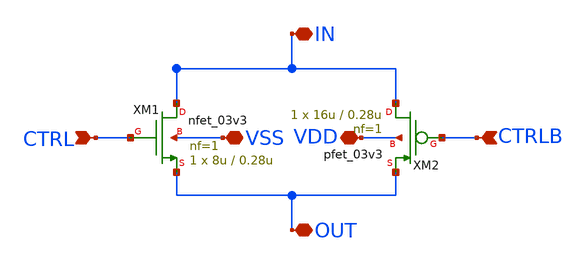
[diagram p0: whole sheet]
** sch_path: designs/libs/core_matchmaker/tg_switch/tg_switch_nmos8u_pmos16u.sch
**.subckt tg_switch_nmos8u_pmos16u IN OUT VSS VDD CTRL CTRLB
*.iopin IN
*.iopin OUT
*.iopin VSS
*.iopin VDD
*.ipin CTRL
*.ipin CTRLB
XM1 IN CTRL OUT VSS nfet_03v3 L=0.28u W=8u nf=1 ad='int((nf+1)/2) * W/nf * 0.18u' as='int((nf+2)/2) * W/nf * 0.18u'
+ pd='2*int((nf+1)/2) * (W/nf + 0.18u)' ps='2*int((nf+2)/2) * (W/nf + 0.18u)' nrd='0.18u / W' nrs='0.18u / W'
+ sa=0 sb=0 sd=0 m=1
XM2 IN CTRLB OUT VDD pfet_03v3 L=0.28u W=16u nf=1 ad='int((nf+1)/2) * W/nf * 0.18u' as='int((nf+2)/2) * W/nf * 0.18u'
+ pd='2*int((nf+1)/2) * (W/nf + 0.18u)' ps='2*int((nf+2)/2) * (W/nf + 0.18u)' nrd='0.18u / W' nrs='0.18u / W'
+ sa=0 sb=0 sd=0 m=1
**.ends
.end
